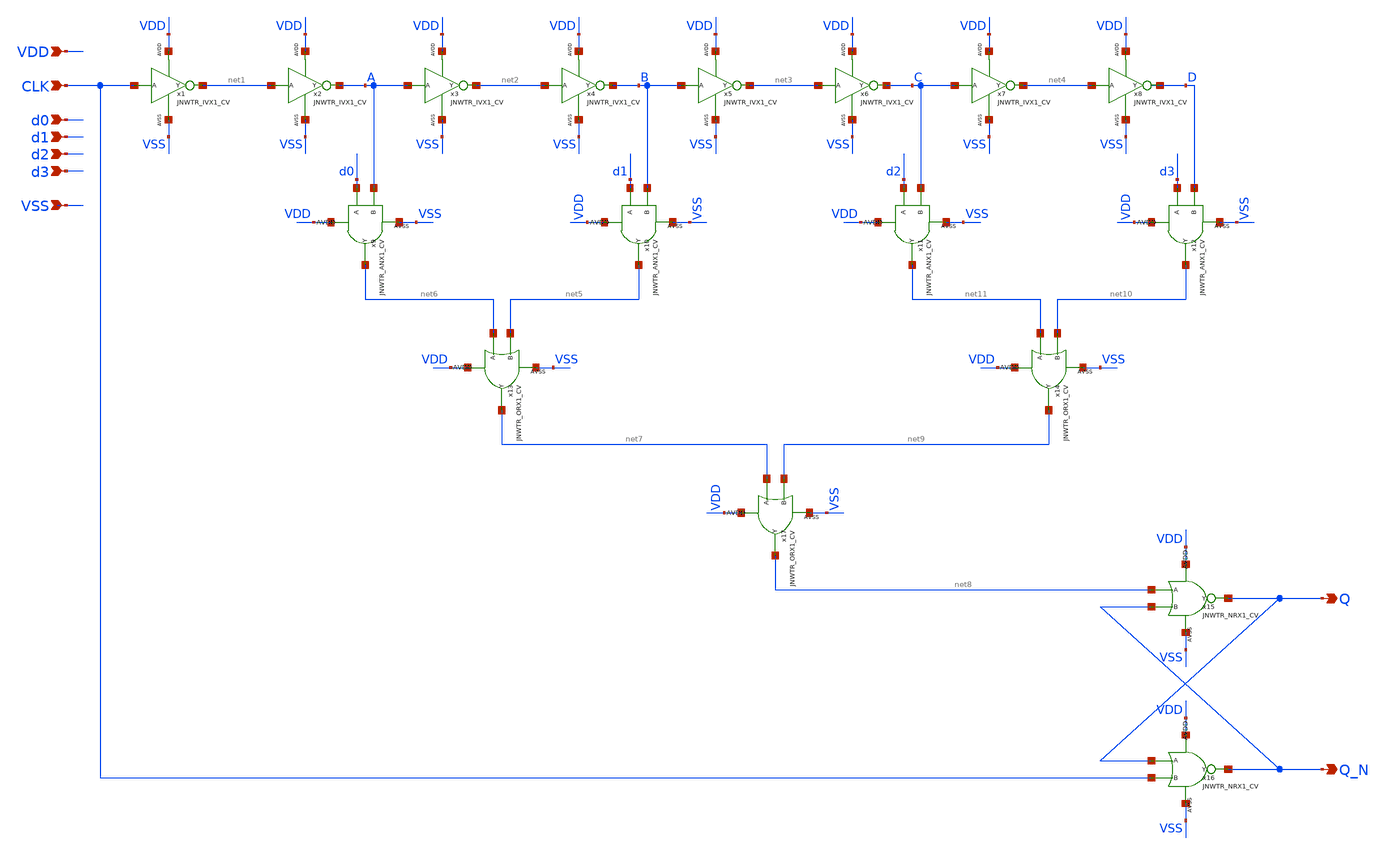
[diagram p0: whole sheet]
** sch_path: design/LELO_TORD_SKY130A/dig-to-time.sch
**.subckt dig-to-time CLK VDD VSS d0 d2 d1 d3 Q Q_N
*.ipin CLK
*.ipin VDD
*.ipin VSS
*.ipin d0
*.ipin d2
*.ipin d1
*.ipin d3
*.opin Q
*.opin Q_N
x1 CLK net1 VDD VSS JNWTR_IVX1_CV
x2 net1 A VDD VSS JNWTR_IVX1_CV
x3 A net2 VDD VSS JNWTR_IVX1_CV
x4 net2 B VDD VSS JNWTR_IVX1_CV
x5 B net3 VDD VSS JNWTR_IVX1_CV
x6 net3 C VDD VSS JNWTR_IVX1_CV
x7 C net4 VDD VSS JNWTR_IVX1_CV
x8 net4 D VDD VSS JNWTR_IVX1_CV
x11 d2 C net11 VDD VSS JNWTR_ANX1_CV xoffset=0 yoffset=0 angle=0 M=1
x9 d0 A net6 VDD VSS JNWTR_ANX1_CV xoffset=0 yoffset=0 angle=0 M=1
x17 net7 net9 net8 VDD VSS JNWTR_ORX1_CV xoffset=0 yoffset=0 angle=0 M=1
x14 net11 net10 net9 VDD VSS JNWTR_ORX1_CV xoffset=0 yoffset=0 angle=0 M=1
x10 d1 B net5 VDD VSS JNWTR_ANX1_CV xoffset=0 yoffset=0 angle=0 M=1
x12 d3 D net10 VDD VSS JNWTR_ANX1_CV xoffset=0 yoffset=0 angle=0 M=1
x13 net6 net5 net7 VDD VSS JNWTR_ORX1_CV xoffset=0 yoffset=0 angle=0 M=1
x15 net8 Q_N Q VDD VSS JNWTR_NRX1_CV
x16 Q CLK Q_N VDD VSS JNWTR_NRX1_CV
**.ends
.end
